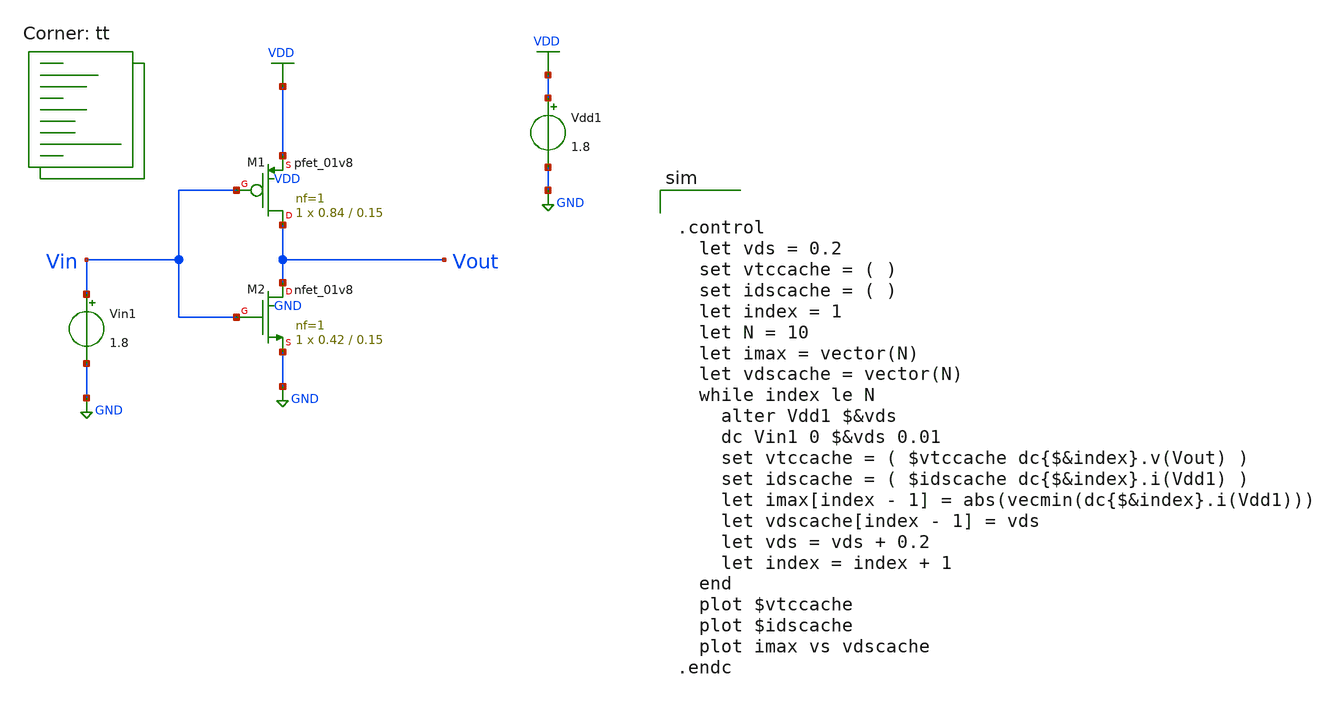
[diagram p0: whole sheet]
** sch_path: tutorial-2/source/q1c.sch
**.subckt q1c
XM1 Vout Vin VDD VDD sky130_fd_pr__pfet_01v8 L=0.15 W=0.84 nf=1 ad='int((nf+1)/2) * W/nf * 0.29' as='int((nf+2)/2) * W/nf * 0.29'
+ pd='2*int((nf+1)/2) * (W/nf + 0.29)' ps='2*int((nf+2)/2) * (W/nf + 0.29)' nrd='0.29 / W' nrs='0.29 / W'
+ sa=0 sb=0 sd=0 mult=1 m=1
XM2 Vout Vin GND GND sky130_fd_pr__nfet_01v8 L=0.15 W=0.42 nf=1 ad='int((nf+1)/2) * W/nf * 0.29' as='int((nf+2)/2) * W/nf * 0.29'
+ pd='2*int((nf+1)/2) * (W/nf + 0.29)' ps='2*int((nf+2)/2) * (W/nf + 0.29)' nrd='0.29 / W' nrs='0.29 / W'
+ sa=0 sb=0 sd=0 mult=1 m=1
Vdd1 VDD GND 1.8
Vin1 Vin GND 1.8
**** begin user architecture code
.lib $::SKYWATER_MODELS/sky130.lib.spice tt


.control
  let vds = 0.2
  set vtccache = ( )
  set idscache = ( )
  let index = 1
  let N = 10
  let imax = vector(N)
  let vdscache = vector(N)
  while index le N
    alter Vdd1 $&vds
    dc Vin1 0 $&vds 0.01
    set vtccache = ( $vtccache dc{$&index}.v(Vout) )
    set idscache = ( $idscache dc{$&index}.i(Vdd1) )
    let imax[index - 1] = abs(vecmin(dc{$&index}.i(Vdd1)))
    let vdscache[index - 1] = vds
    let vds = vds + 0.2
    let index = index + 1
  end
  plot $vtccache
  plot $idscache
  plot imax vs vdscache
.endc

**** end user architecture code
**.ends
.GLOBAL VDD
.GLOBAL GND
.end
